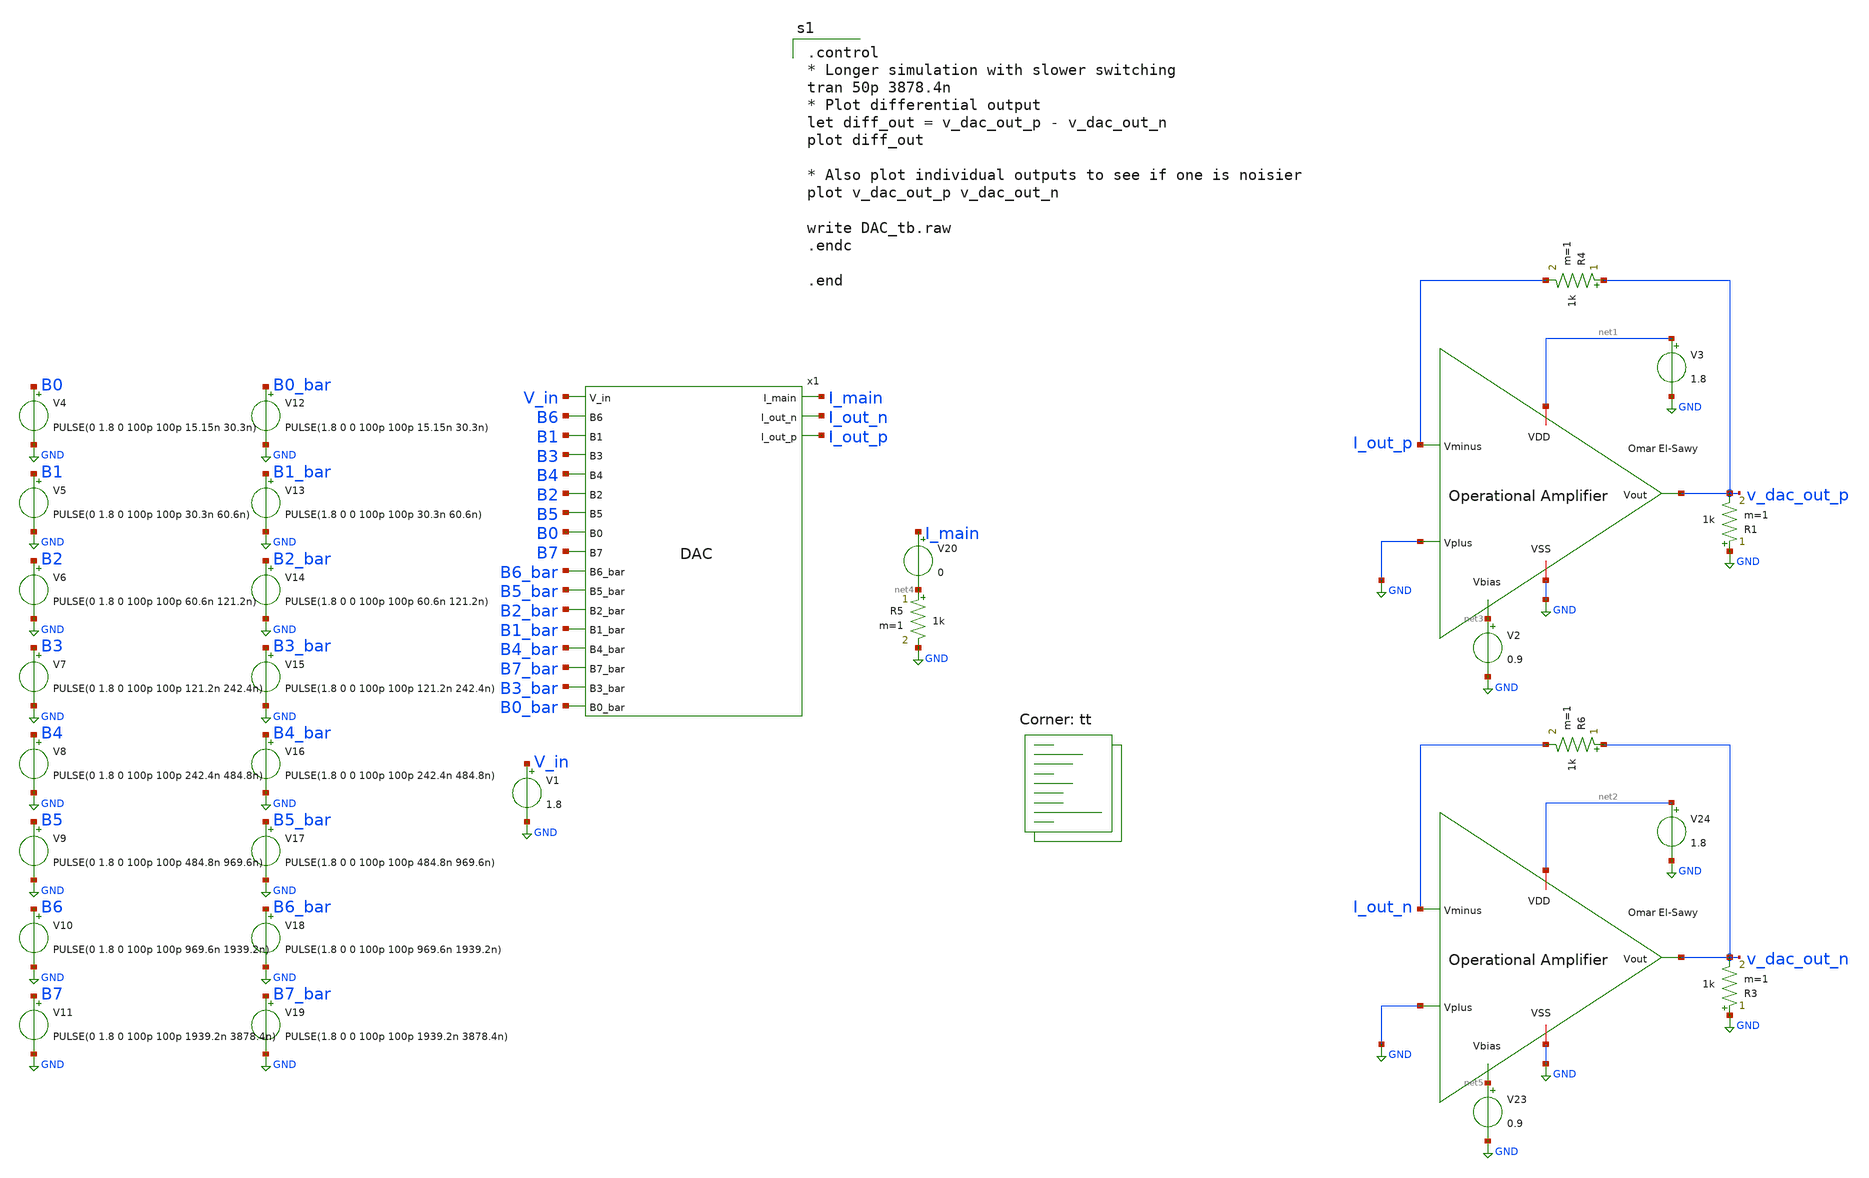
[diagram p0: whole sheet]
** sch_path: analog/schematics/components/DAC/unit_tb/DAC_tb.sch
**.subckt DAC_tb
x1 V_in I_main I_out_n I_out_p B6 B1 B3 B4 B2 B5 B0 B7 B6_bar B5_bar B2_bar B1_bar B4_bar B7_bar
+ B3_bar B0_bar DAC
V4 B0 GND PULSE(0 1.8 0 100p 100p 15.15n 30.3n)
V5 B1 GND PULSE(0 1.8 0 100p 100p 30.3n 60.6n)
V6 B2 GND PULSE(0 1.8 0 100p 100p 60.6n 121.2n)
V7 B3 GND PULSE(0 1.8 0 100p 100p 121.2n 242.4n)
V8 B4 GND PULSE(0 1.8 0 100p 100p 242.4n 484.8n)
V9 B5 GND PULSE(0 1.8 0 100p 100p 484.8n 969.6n)
V10 B6 GND PULSE(0 1.8 0 100p 100p 969.6n 1939.2n)
V11 B7 GND PULSE(0 1.8 0 100p 100p 1939.2n 3878.4n)
V12 B0_bar GND PULSE(1.8 0 0 100p 100p 15.15n 30.3n)
V13 B1_bar GND PULSE(1.8 0 0 100p 100p 30.3n 60.6n)
V14 B2_bar GND PULSE(1.8 0 0 100p 100p 60.6n 121.2n)
V15 B3_bar GND PULSE(1.8 0 0 100p 100p 121.2n 242.4n)
V16 B4_bar GND PULSE(1.8 0 0 100p 100p 242.4n 484.8n)
V17 B5_bar GND PULSE(1.8 0 0 100p 100p 484.8n 969.6n)
V18 B6_bar GND PULSE(1.8 0 0 100p 100p 969.6n 1939.2n)
V19 B7_bar GND PULSE(1.8 0 0 100p 100p 1939.2n 3878.4n)
V1 V_in GND 1.8
x2 net1 v_dac_out_p I_out_p GND net3 GND OpAmp
V2 net3 GND 0.9
V3 net1 GND 1.8
R4 v_dac_out_p I_out_p 1k m=1
R1 GND v_dac_out_p 1k m=1
V20 I_main net4 0
R5 net4 GND 1k m=1
x3 net2 v_dac_out_n I_out_n GND net5 GND OpAmp
V23 net5 GND 0.9
V24 net2 GND 1.8
R6 v_dac_out_n I_out_n 1k m=1
R3 GND v_dac_out_n 1k m=1
**** begin user architecture code
.lib $::SKYWATER_MODELS/sky130.lib.spice tt

.control
* Longer simulation with slower switching
tran 50p 3878.4n
* Plot differential output
let diff_out = v_dac_out_p - v_dac_out_n
plot diff_out

* Also plot individual outputs to see if one is noisier
plot v_dac_out_p v_dac_out_n

write DAC_tb.raw
.endc

.end

**** end user architecture code
**.ends

* expanding   symbol:  DAC.sym # of pins=20
** sym_path: analog/schematics/DAC.sym
** sch_path: analog/schematics/DAC.sch
.subckt DAC V_in I_main I_out_n I_out_p B6 B1 B3 B4 B2 B5 B0 B7 B6_bar B5_bar B2_bar B1_bar B4_bar
+ B7_bar B3_bar B0_bar
*.ipin B0
*.ipin V_in
*.ipin B0_bar
*.ipin B1
*.ipin B2
*.ipin B3
*.ipin B1_bar
*.ipin B2_bar
*.ipin B3_bar
*.ipin B4
*.ipin B4_bar
*.ipin B5
*.ipin B6
*.ipin B7
*.ipin B5_bar
*.ipin B6_bar
*.ipin B7_bar
*.opin I_main
*.opin I_out_p
*.opin I_out_n
XM1 net2 net1 V_in V_in sky130_fd_pr__pfet_01v8 L=0.15 W=84 nf=1 ad='int((nf+1)/2) * W/nf * 0.29' as='int((nf+2)/2) * W/nf * 0.29'
+ pd='2*int((nf+1)/2) * (W/nf + 0.29)' ps='2*int((nf+2)/2) * (W/nf + 0.29)' nrd='0.29 / W' nrs='0.29 / W'
+ sa=0 sb=0 sd=0 mult=1 m=1
XM2 net6 I_main net2 net2 sky130_fd_pr__pfet_01v8 L=0.15 W=84 nf=1 ad='int((nf+1)/2) * W/nf * 0.29' as='int((nf+2)/2) * W/nf * 0.29'
+ pd='2*int((nf+1)/2) * (W/nf + 0.29)' ps='2*int((nf+2)/2) * (W/nf + 0.29)' nrd='0.29 / W' nrs='0.29 / W'
+ sa=0 sb=0 sd=0 mult=1 m=1
XM3 net1 net1 V_in V_in sky130_fd_pr__pfet_01v8 L=0.15 W=84 nf=1 ad='int((nf+1)/2) * W/nf * 0.29' as='int((nf+2)/2) * W/nf * 0.29'
+ pd='2*int((nf+1)/2) * (W/nf + 0.29)' ps='2*int((nf+2)/2) * (W/nf + 0.29)' nrd='0.29 / W' nrs='0.29 / W'
+ sa=0 sb=0 sd=0 mult=1 m=1
XM4 I_main I_main net1 net1 sky130_fd_pr__pfet_01v8 L=0.15 W=84 nf=1 ad='int((nf+1)/2) * W/nf * 0.29'
+ as='int((nf+2)/2) * W/nf * 0.29' pd='2*int((nf+1)/2) * (W/nf + 0.29)' ps='2*int((nf+2)/2) * (W/nf + 0.29)'
+ nrd='0.29 / W' nrs='0.29 / W' sa=0 sb=0 sd=0 mult=1 m=1
XM5 net3 net1 V_in V_in sky130_fd_pr__pfet_01v8 L=0.15 W=42 nf=1 ad='int((nf+1)/2) * W/nf * 0.29' as='int((nf+2)/2) * W/nf * 0.29'
+ pd='2*int((nf+1)/2) * (W/nf + 0.29)' ps='2*int((nf+2)/2) * (W/nf + 0.29)' nrd='0.29 / W' nrs='0.29 / W'
+ sa=0 sb=0 sd=0 mult=1 m=1
XM6 net7 I_main net3 net3 sky130_fd_pr__pfet_01v8 L=0.15 W=42 nf=1 ad='int((nf+1)/2) * W/nf * 0.29' as='int((nf+2)/2) * W/nf * 0.29'
+ pd='2*int((nf+1)/2) * (W/nf + 0.29)' ps='2*int((nf+2)/2) * (W/nf + 0.29)' nrd='0.29 / W' nrs='0.29 / W'
+ sa=0 sb=0 sd=0 mult=1 m=1
XM7 net4 net1 V_in V_in sky130_fd_pr__pfet_01v8 L=0.15 W=21 nf=1 ad='int((nf+1)/2) * W/nf * 0.29' as='int((nf+2)/2) * W/nf * 0.29'
+ pd='2*int((nf+1)/2) * (W/nf + 0.29)' ps='2*int((nf+2)/2) * (W/nf + 0.29)' nrd='0.29 / W' nrs='0.29 / W'
+ sa=0 sb=0 sd=0 mult=1 m=1
XM8 net8 I_main net4 net4 sky130_fd_pr__pfet_01v8 L=0.15 W=21 nf=1 ad='int((nf+1)/2) * W/nf * 0.29' as='int((nf+2)/2) * W/nf * 0.29'
+ pd='2*int((nf+1)/2) * (W/nf + 0.29)' ps='2*int((nf+2)/2) * (W/nf + 0.29)' nrd='0.29 / W' nrs='0.29 / W'
+ sa=0 sb=0 sd=0 mult=1 m=1
XM9 net5 net1 V_in V_in sky130_fd_pr__pfet_01v8 L=0.15 W=10.5 nf=1 ad='int((nf+1)/2) * W/nf * 0.29' as='int((nf+2)/2) * W/nf * 0.29'
+ pd='2*int((nf+1)/2) * (W/nf + 0.29)' ps='2*int((nf+2)/2) * (W/nf + 0.29)' nrd='0.29 / W' nrs='0.29 / W'
+ sa=0 sb=0 sd=0 mult=1 m=1
XM10 net9 I_main net5 net5 sky130_fd_pr__pfet_01v8 L=0.15 W=10.5 nf=1 ad='int((nf+1)/2) * W/nf * 0.29'
+ as='int((nf+2)/2) * W/nf * 0.29' pd='2*int((nf+1)/2) * (W/nf + 0.29)' ps='2*int((nf+2)/2) * (W/nf + 0.29)'
+ nrd='0.29 / W' nrs='0.29 / W' sa=0 sb=0 sd=0 mult=1 m=1
XM12 I_out_p B0 net6 net6 sky130_fd_pr__pfet_01v8 L=0.15 W=1 nf=1 ad='int((nf+1)/2) * W/nf * 0.29' as='int((nf+2)/2) * W/nf * 0.29'
+ pd='2*int((nf+1)/2) * (W/nf + 0.29)' ps='2*int((nf+2)/2) * (W/nf + 0.29)' nrd='0.29 / W' nrs='0.29 / W'
+ sa=0 sb=0 sd=0 mult=1 m=1
XM13 I_out_n B0_bar net6 net6 sky130_fd_pr__pfet_01v8 L=0.15 W=1 nf=1 ad='int((nf+1)/2) * W/nf * 0.29'
+ as='int((nf+2)/2) * W/nf * 0.29' pd='2*int((nf+1)/2) * (W/nf + 0.29)' ps='2*int((nf+2)/2) * (W/nf + 0.29)'
+ nrd='0.29 / W' nrs='0.29 / W' sa=0 sb=0 sd=0 mult=1 m=1
XM14 I_out_p B1 net7 net7 sky130_fd_pr__pfet_01v8 L=0.15 W=1 nf=1 ad='int((nf+1)/2) * W/nf * 0.29' as='int((nf+2)/2) * W/nf * 0.29'
+ pd='2*int((nf+1)/2) * (W/nf + 0.29)' ps='2*int((nf+2)/2) * (W/nf + 0.29)' nrd='0.29 / W' nrs='0.29 / W'
+ sa=0 sb=0 sd=0 mult=1 m=1
XM15 I_out_n B1_bar net7 net7 sky130_fd_pr__pfet_01v8 L=0.15 W=1 nf=1 ad='int((nf+1)/2) * W/nf * 0.29'
+ as='int((nf+2)/2) * W/nf * 0.29' pd='2*int((nf+1)/2) * (W/nf + 0.29)' ps='2*int((nf+2)/2) * (W/nf + 0.29)'
+ nrd='0.29 / W' nrs='0.29 / W' sa=0 sb=0 sd=0 mult=1 m=1
XM16 I_out_p B2 net8 net8 sky130_fd_pr__pfet_01v8 L=0.15 W=1 nf=1 ad='int((nf+1)/2) * W/nf * 0.29' as='int((nf+2)/2) * W/nf * 0.29'
+ pd='2*int((nf+1)/2) * (W/nf + 0.29)' ps='2*int((nf+2)/2) * (W/nf + 0.29)' nrd='0.29 / W' nrs='0.29 / W'
+ sa=0 sb=0 sd=0 mult=1 m=1
XM17 I_out_n B2_bar net8 net8 sky130_fd_pr__pfet_01v8 L=0.15 W=1 nf=1 ad='int((nf+1)/2) * W/nf * 0.29'
+ as='int((nf+2)/2) * W/nf * 0.29' pd='2*int((nf+1)/2) * (W/nf + 0.29)' ps='2*int((nf+2)/2) * (W/nf + 0.29)'
+ nrd='0.29 / W' nrs='0.29 / W' sa=0 sb=0 sd=0 mult=1 m=1
XM18 I_out_p B3 net9 net9 sky130_fd_pr__pfet_01v8 L=0.15 W=1 nf=1 ad='int((nf+1)/2) * W/nf * 0.29' as='int((nf+2)/2) * W/nf * 0.29'
+ pd='2*int((nf+1)/2) * (W/nf + 0.29)' ps='2*int((nf+2)/2) * (W/nf + 0.29)' nrd='0.29 / W' nrs='0.29 / W'
+ sa=0 sb=0 sd=0 mult=1 m=1
XM19 I_out_n B3_bar net9 net9 sky130_fd_pr__pfet_01v8 L=0.15 W=1 nf=1 ad='int((nf+1)/2) * W/nf * 0.29'
+ as='int((nf+2)/2) * W/nf * 0.29' pd='2*int((nf+1)/2) * (W/nf + 0.29)' ps='2*int((nf+2)/2) * (W/nf + 0.29)'
+ nrd='0.29 / W' nrs='0.29 / W' sa=0 sb=0 sd=0 mult=1 m=1
XM11 net10 net1 V_in V_in sky130_fd_pr__pfet_01v8 L=0.15 W=5.25 nf=1 ad='int((nf+1)/2) * W/nf * 0.29'
+ as='int((nf+2)/2) * W/nf * 0.29' pd='2*int((nf+1)/2) * (W/nf + 0.29)' ps='2*int((nf+2)/2) * (W/nf + 0.29)'
+ nrd='0.29 / W' nrs='0.29 / W' sa=0 sb=0 sd=0 mult=1 m=1
XM20 net14 I_main net10 net10 sky130_fd_pr__pfet_01v8 L=0.15 W=5.25 nf=1 ad='int((nf+1)/2) * W/nf * 0.29'
+ as='int((nf+2)/2) * W/nf * 0.29' pd='2*int((nf+1)/2) * (W/nf + 0.29)' ps='2*int((nf+2)/2) * (W/nf + 0.29)'
+ nrd='0.29 / W' nrs='0.29 / W' sa=0 sb=0 sd=0 mult=1 m=1
XM21 net11 net1 V_in V_in sky130_fd_pr__pfet_01v8 L=0.15 W=2.625 nf=1 ad='int((nf+1)/2) * W/nf * 0.29'
+ as='int((nf+2)/2) * W/nf * 0.29' pd='2*int((nf+1)/2) * (W/nf + 0.29)' ps='2*int((nf+2)/2) * (W/nf + 0.29)'
+ nrd='0.29 / W' nrs='0.29 / W' sa=0 sb=0 sd=0 mult=1 m=1
XM22 net15 I_main net11 net11 sky130_fd_pr__pfet_01v8 L=0.15 W=2.625 nf=1 ad='int((nf+1)/2) * W/nf * 0.29'
+ as='int((nf+2)/2) * W/nf * 0.29' pd='2*int((nf+1)/2) * (W/nf + 0.29)' ps='2*int((nf+2)/2) * (W/nf + 0.29)'
+ nrd='0.29 / W' nrs='0.29 / W' sa=0 sb=0 sd=0 mult=1 m=1
XM23 net12 net1 V_in V_in sky130_fd_pr__pfet_01v8 L=0.15 W=1.3125 nf=1 ad='int((nf+1)/2) * W/nf * 0.29'
+ as='int((nf+2)/2) * W/nf * 0.29' pd='2*int((nf+1)/2) * (W/nf + 0.29)' ps='2*int((nf+2)/2) * (W/nf + 0.29)'
+ nrd='0.29 / W' nrs='0.29 / W' sa=0 sb=0 sd=0 mult=1 m=1
XM24 net16 I_main net12 net12 sky130_fd_pr__pfet_01v8 L=0.15 W=1.3125 nf=1 ad='int((nf+1)/2) * W/nf * 0.29'
+ as='int((nf+2)/2) * W/nf * 0.29' pd='2*int((nf+1)/2) * (W/nf + 0.29)' ps='2*int((nf+2)/2) * (W/nf + 0.29)'
+ nrd='0.29 / W' nrs='0.29 / W' sa=0 sb=0 sd=0 mult=1 m=1
XM25 net13 net1 V_in V_in sky130_fd_pr__pfet_01v8 L=0.15 W=0.65625 nf=1 ad='int((nf+1)/2) * W/nf * 0.29'
+ as='int((nf+2)/2) * W/nf * 0.29' pd='2*int((nf+1)/2) * (W/nf + 0.29)' ps='2*int((nf+2)/2) * (W/nf + 0.29)'
+ nrd='0.29 / W' nrs='0.29 / W' sa=0 sb=0 sd=0 mult=1 m=1
XM26 net17 I_main net13 net13 sky130_fd_pr__pfet_01v8 L=0.15 W=0.65625 nf=1 ad='int((nf+1)/2) * W/nf * 0.29'
+ as='int((nf+2)/2) * W/nf * 0.29' pd='2*int((nf+1)/2) * (W/nf + 0.29)' ps='2*int((nf+2)/2) * (W/nf + 0.29)'
+ nrd='0.29 / W' nrs='0.29 / W' sa=0 sb=0 sd=0 mult=1 m=1
XM27 I_out_p B4 net14 net14 sky130_fd_pr__pfet_01v8 L=0.15 W=1 nf=1 ad='int((nf+1)/2) * W/nf * 0.29'
+ as='int((nf+2)/2) * W/nf * 0.29' pd='2*int((nf+1)/2) * (W/nf + 0.29)' ps='2*int((nf+2)/2) * (W/nf + 0.29)'
+ nrd='0.29 / W' nrs='0.29 / W' sa=0 sb=0 sd=0 mult=1 m=1
XM28 I_out_n B4_bar net14 net14 sky130_fd_pr__pfet_01v8 L=0.15 W=1 nf=1 ad='int((nf+1)/2) * W/nf * 0.29'
+ as='int((nf+2)/2) * W/nf * 0.29' pd='2*int((nf+1)/2) * (W/nf + 0.29)' ps='2*int((nf+2)/2) * (W/nf + 0.29)'
+ nrd='0.29 / W' nrs='0.29 / W' sa=0 sb=0 sd=0 mult=1 m=1
XM29 I_out_p B5 net15 net15 sky130_fd_pr__pfet_01v8 L=0.15 W=1 nf=1 ad='int((nf+1)/2) * W/nf * 0.29'
+ as='int((nf+2)/2) * W/nf * 0.29' pd='2*int((nf+1)/2) * (W/nf + 0.29)' ps='2*int((nf+2)/2) * (W/nf + 0.29)'
+ nrd='0.29 / W' nrs='0.29 / W' sa=0 sb=0 sd=0 mult=1 m=1
XM30 I_out_n B5_bar net15 net15 sky130_fd_pr__pfet_01v8 L=0.15 W=1 nf=1 ad='int((nf+1)/2) * W/nf * 0.29'
+ as='int((nf+2)/2) * W/nf * 0.29' pd='2*int((nf+1)/2) * (W/nf + 0.29)' ps='2*int((nf+2)/2) * (W/nf + 0.29)'
+ nrd='0.29 / W' nrs='0.29 / W' sa=0 sb=0 sd=0 mult=1 m=1
XM31 I_out_p B6 net16 net16 sky130_fd_pr__pfet_01v8 L=0.15 W=1 nf=1 ad='int((nf+1)/2) * W/nf * 0.29'
+ as='int((nf+2)/2) * W/nf * 0.29' pd='2*int((nf+1)/2) * (W/nf + 0.29)' ps='2*int((nf+2)/2) * (W/nf + 0.29)'
+ nrd='0.29 / W' nrs='0.29 / W' sa=0 sb=0 sd=0 mult=1 m=1
XM32 I_out_n B6_bar net16 net16 sky130_fd_pr__pfet_01v8 L=0.15 W=1 nf=1 ad='int((nf+1)/2) * W/nf * 0.29'
+ as='int((nf+2)/2) * W/nf * 0.29' pd='2*int((nf+1)/2) * (W/nf + 0.29)' ps='2*int((nf+2)/2) * (W/nf + 0.29)'
+ nrd='0.29 / W' nrs='0.29 / W' sa=0 sb=0 sd=0 mult=1 m=1
XM33 I_out_p B7 net17 net17 sky130_fd_pr__pfet_01v8 L=0.15 W=1 nf=1 ad='int((nf+1)/2) * W/nf * 0.29'
+ as='int((nf+2)/2) * W/nf * 0.29' pd='2*int((nf+1)/2) * (W/nf + 0.29)' ps='2*int((nf+2)/2) * (W/nf + 0.29)'
+ nrd='0.29 / W' nrs='0.29 / W' sa=0 sb=0 sd=0 mult=1 m=1
XM34 I_out_n B7_bar net17 net17 sky130_fd_pr__pfet_01v8 L=0.15 W=1 nf=1 ad='int((nf+1)/2) * W/nf * 0.29'
+ as='int((nf+2)/2) * W/nf * 0.29' pd='2*int((nf+1)/2) * (W/nf + 0.29)' ps='2*int((nf+2)/2) * (W/nf + 0.29)'
+ nrd='0.29 / W' nrs='0.29 / W' sa=0 sb=0 sd=0 mult=1 m=1
.ends


* expanding   symbol:  OpAmps/template/OpAmp.sym # of pins=6
** sym_path: OpAmps/template/OpAmp.sym
** sch_path: OpAmps/template/OpAmp.sch
.subckt OpAmp VDD Vout Vminus Vplus Vbias VSS
*.ipin Vplus
*.ipin Vminus
*.iopin VDD
*.iopin VSS
*.ipin Vbias
*.opin Vout
XM1 net2 Vminus net1 VSS sky130_fd_pr__nfet_01v8 L=0.15 W=16 nf=1 ad='int((nf+1)/2) * W/nf * 0.29' as='int((nf+2)/2) * W/nf * 0.29'
+ pd='2*int((nf+1)/2) * (W/nf + 0.29)' ps='2*int((nf+2)/2) * (W/nf + 0.29)' nrd='0.29 / W' nrs='0.29 / W'
+ sa=0 sb=0 sd=0 mult=1 m=1
XM2 net3 Vplus net1 VSS sky130_fd_pr__nfet_01v8 L=0.15 W=16 nf=1 ad='int((nf+1)/2) * W/nf * 0.29' as='int((nf+2)/2) * W/nf * 0.29'
+ pd='2*int((nf+1)/2) * (W/nf + 0.29)' ps='2*int((nf+2)/2) * (W/nf + 0.29)' nrd='0.29 / W' nrs='0.29 / W'
+ sa=0 sb=0 sd=0 mult=1 m=1
XM3 net2 net2 VDD VDD sky130_fd_pr__pfet_01v8 L=0.4 W=1 nf=1 ad='int((nf+1)/2) * W/nf * 0.29' as='int((nf+2)/2) * W/nf * 0.29'
+ pd='2*int((nf+1)/2) * (W/nf + 0.29)' ps='2*int((nf+2)/2) * (W/nf + 0.29)' nrd='0.29 / W' nrs='0.29 / W'
+ sa=0 sb=0 sd=0 mult=1 m=1
XM4 net3 net2 VDD VDD sky130_fd_pr__pfet_01v8 L=0.4 W=1 nf=1 ad='int((nf+1)/2) * W/nf * 0.29' as='int((nf+2)/2) * W/nf * 0.29'
+ pd='2*int((nf+1)/2) * (W/nf + 0.29)' ps='2*int((nf+2)/2) * (W/nf + 0.29)' nrd='0.29 / W' nrs='0.29 / W'
+ sa=0 sb=0 sd=0 mult=1 m=1
XM5 net1 Vbias VSS VSS sky130_fd_pr__nfet_01v8 L=0.30 W=2 nf=1 ad='int((nf+1)/2) * W/nf * 0.29' as='int((nf+2)/2) * W/nf * 0.29'
+ pd='2*int((nf+1)/2) * (W/nf + 0.29)' ps='2*int((nf+2)/2) * (W/nf + 0.29)' nrd='0.29 / W' nrs='0.29 / W'
+ sa=0 sb=0 sd=0 mult=1 m=1
XM6 Vout net3 VDD VDD sky130_fd_pr__pfet_01v8 L=0.40 W=1 nf=1 ad='int((nf+1)/2) * W/nf * 0.29' as='int((nf+2)/2) * W/nf * 0.29'
+ pd='2*int((nf+1)/2) * (W/nf + 0.29)' ps='2*int((nf+2)/2) * (W/nf + 0.29)' nrd='0.29 / W' nrs='0.29 / W'
+ sa=0 sb=0 sd=0 mult=1 m=1
XC1 Vout net3 sky130_fd_pr__cap_mim_m3_1 W=1 L=1 MF=1 m=1
XM7 Vout Vbias VSS VSS sky130_fd_pr__nfet_01v8 L=0.3 W=1 nf=1 ad='int((nf+1)/2) * W/nf * 0.29' as='int((nf+2)/2) * W/nf * 0.29'
+ pd='2*int((nf+1)/2) * (W/nf + 0.29)' ps='2*int((nf+2)/2) * (W/nf + 0.29)' nrd='0.29 / W' nrs='0.29 / W'
+ sa=0 sb=0 sd=0 mult=1 m=1
.ends

.GLOBAL GND
.GLOBAL VDD
.GLOBAL VSS
.end
